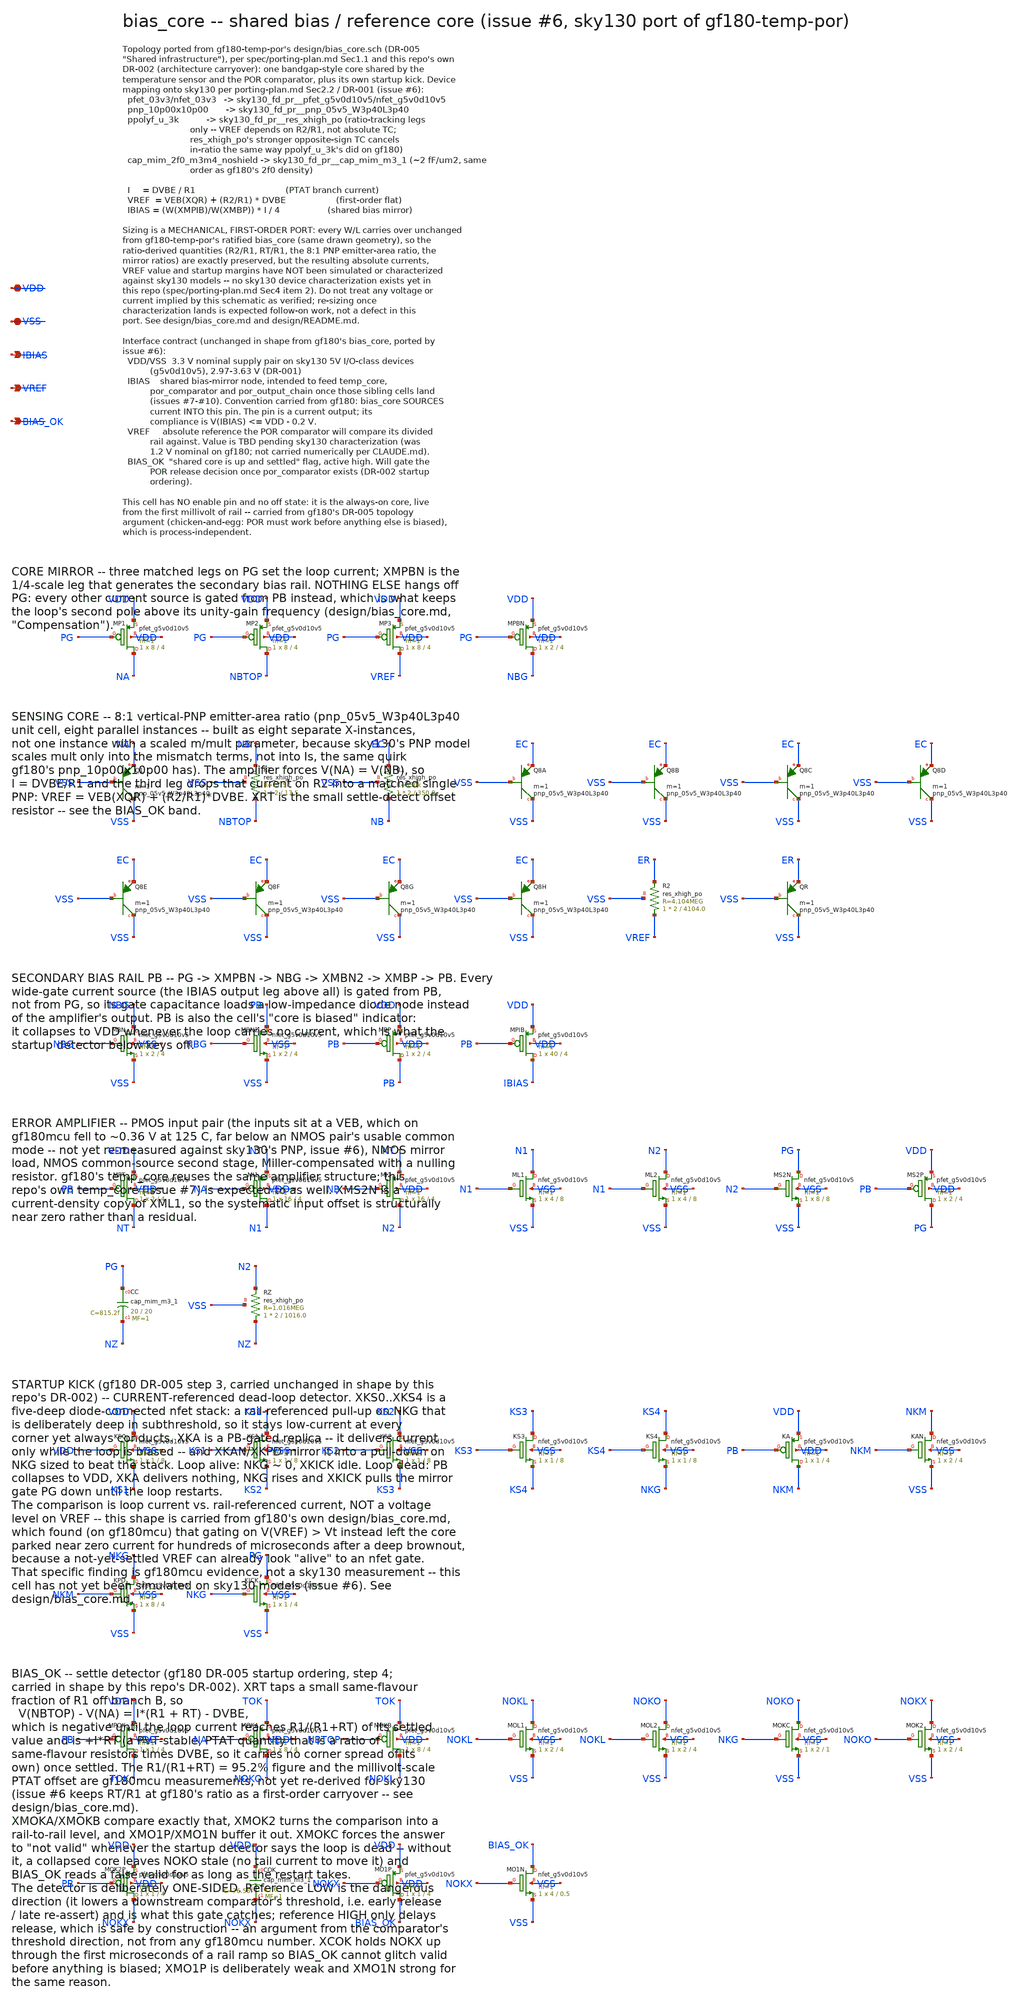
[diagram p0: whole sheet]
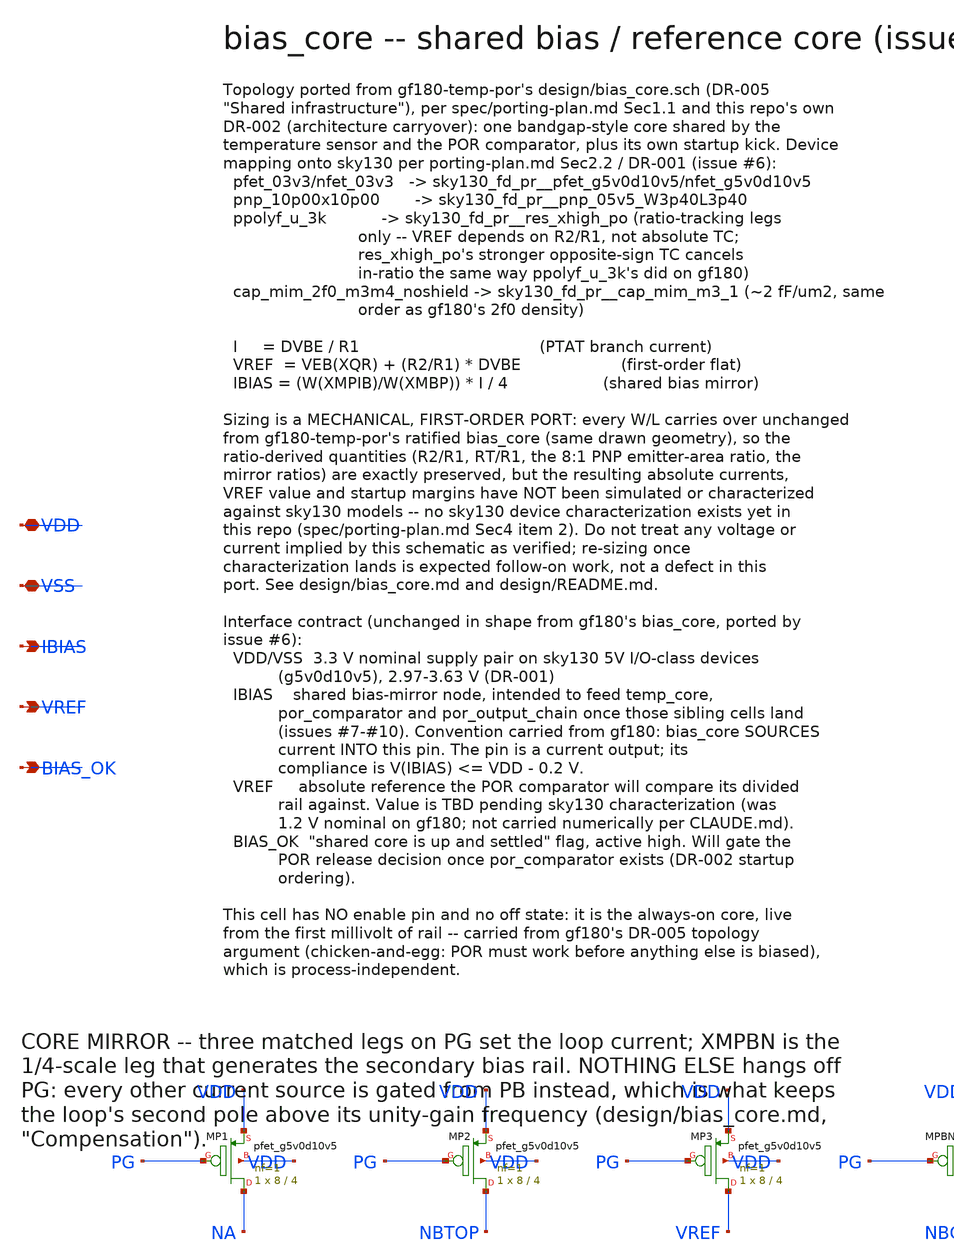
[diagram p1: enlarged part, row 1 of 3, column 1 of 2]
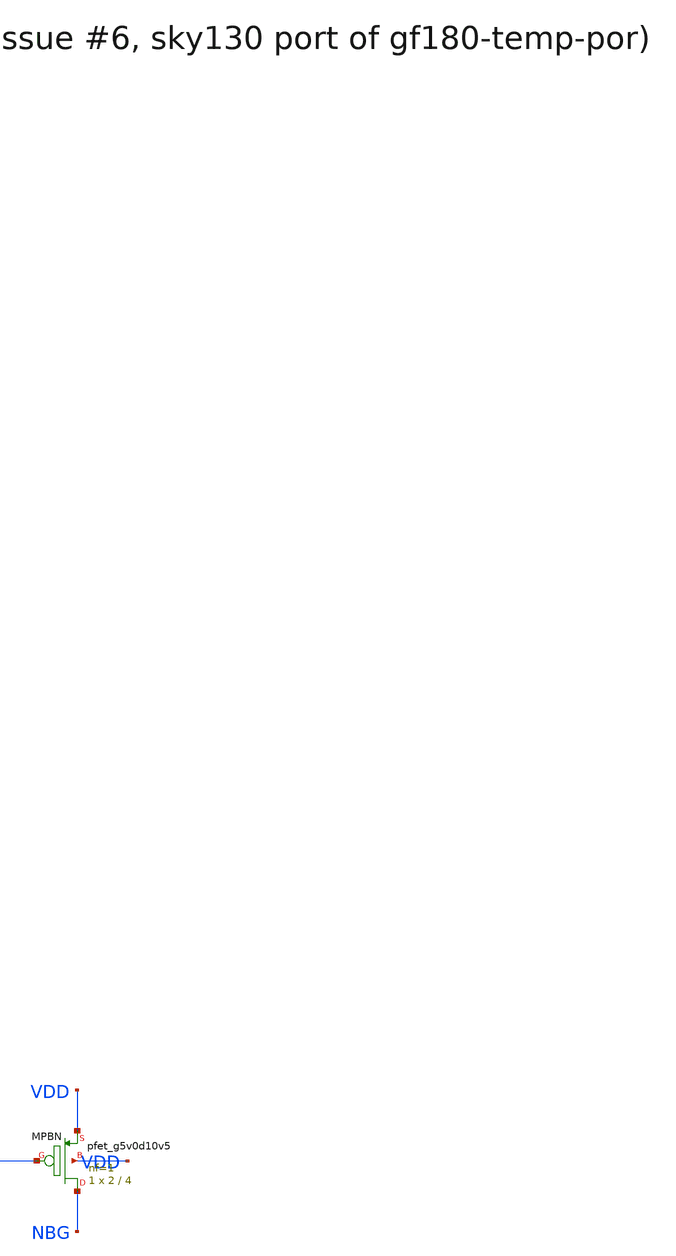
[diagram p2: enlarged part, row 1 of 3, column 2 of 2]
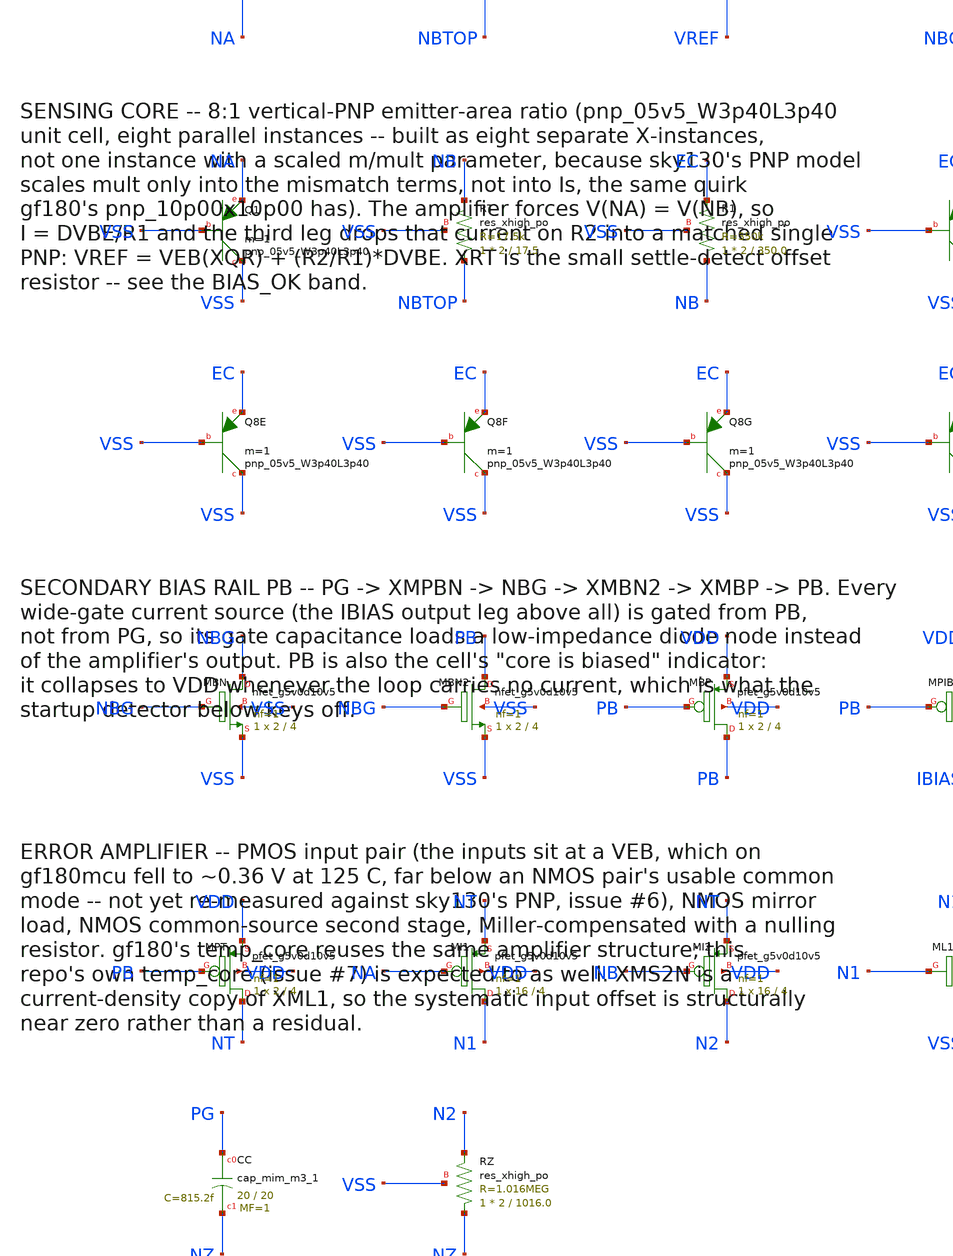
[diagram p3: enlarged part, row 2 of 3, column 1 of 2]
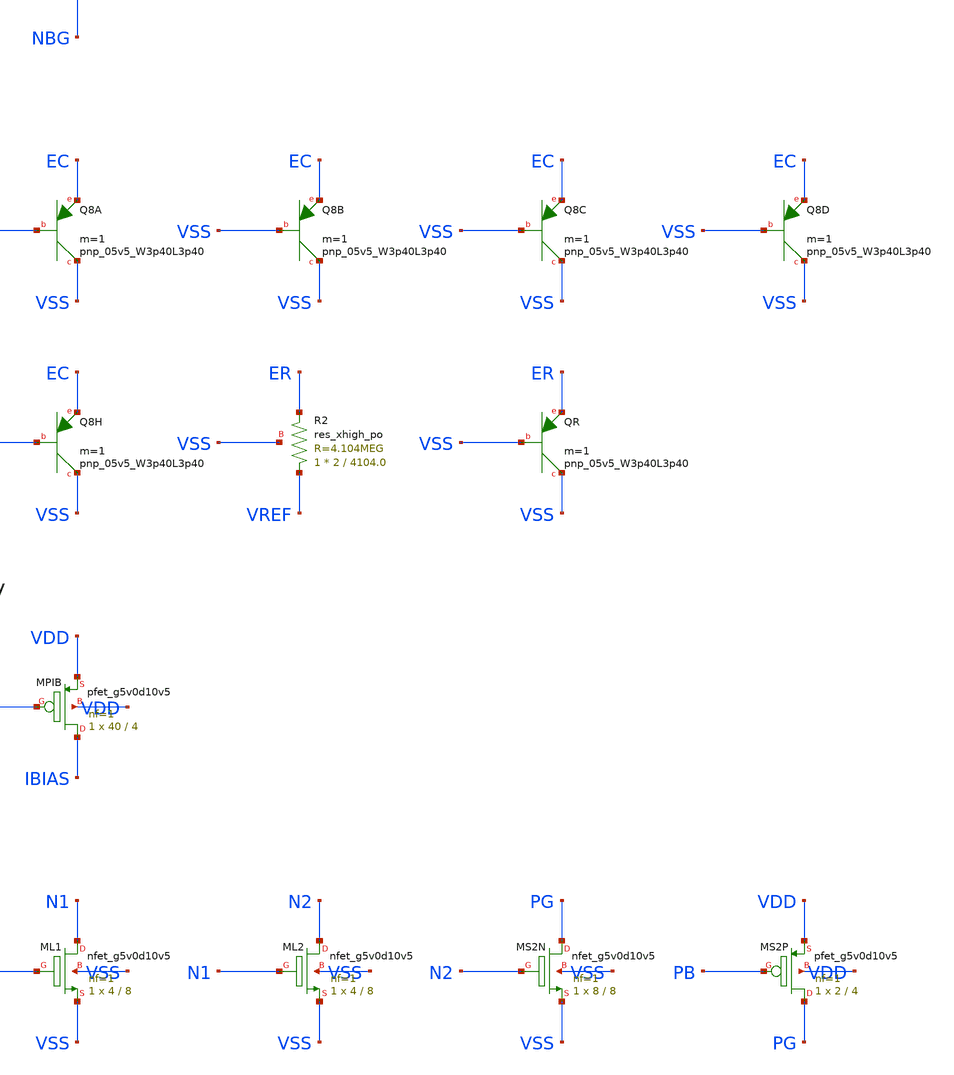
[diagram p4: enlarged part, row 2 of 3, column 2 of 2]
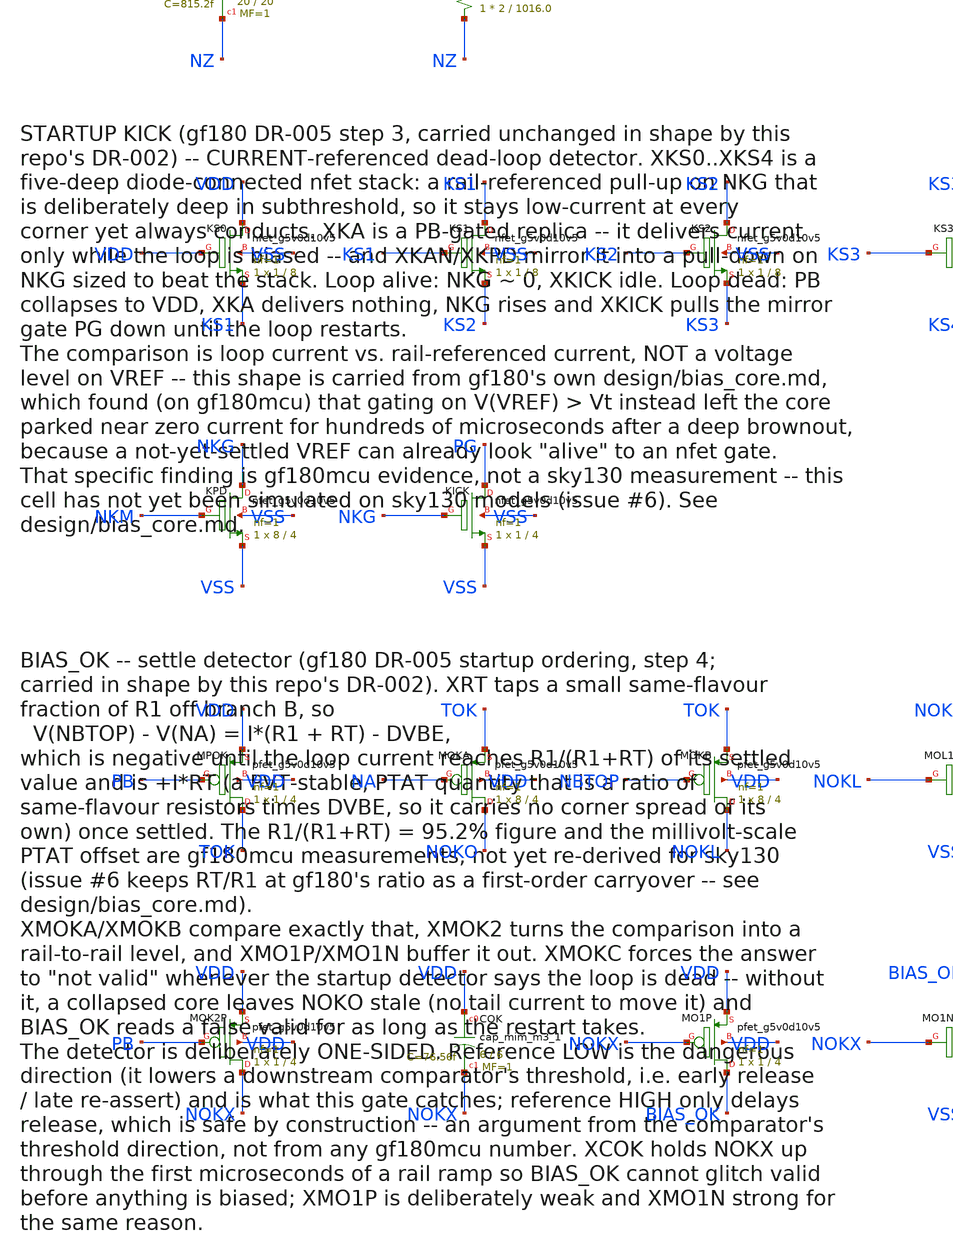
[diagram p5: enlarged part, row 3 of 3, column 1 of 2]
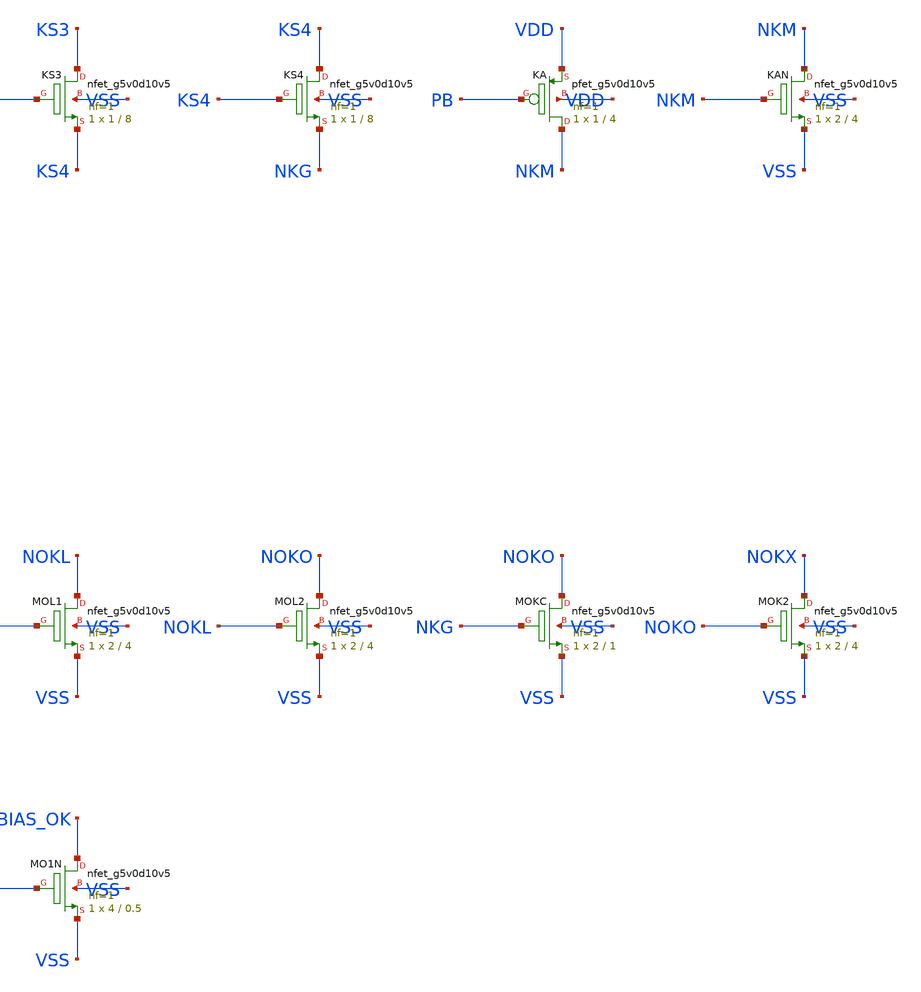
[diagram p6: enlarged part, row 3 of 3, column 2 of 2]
** sch_path: design/bias_core.sch
**.subckt bias_core VDD VSS IBIAS VREF BIAS_OK
*.iopin VDD
*.iopin VSS
*.opin IBIAS
*.opin VREF
*.opin BIAS_OK
XMP1 NA PG VDD VDD sky130_fd_pr__pfet_g5v0d10v5 L=4 W=8 nf=1 ad='int((1 + 1)/2) * 8 / 1 * 0.29' as='int((1 + 2)/2) * 8 / 1 * 0.29'
+ pd='2*int((1 + 1)/2) * (8 / 1 + 0.29)' ps='2*int((1 + 2)/2) * (8 / 1 + 0.29)' nrd='0.29 / 8 ' nrs='0.29 / 8 '
+ sa=0 sb=0 sd=0 mult=1 m=1
XMP2 NBTOP PG VDD VDD sky130_fd_pr__pfet_g5v0d10v5 L=4 W=8 nf=1 ad='int((1 + 1)/2) * 8 / 1 * 0.29' as='int((1 + 2)/2) * 8 / 1 * 0.29'
+ pd='2*int((1 + 1)/2) * (8 / 1 + 0.29)' ps='2*int((1 + 2)/2) * (8 / 1 + 0.29)' nrd='0.29 / 8 ' nrs='0.29 / 8 '
+ sa=0 sb=0 sd=0 mult=1 m=1
XMP3 VREF PG VDD VDD sky130_fd_pr__pfet_g5v0d10v5 L=4 W=8 nf=1 ad='int((1 + 1)/2) * 8 / 1 * 0.29' as='int((1 + 2)/2) * 8 / 1 * 0.29'
+ pd='2*int((1 + 1)/2) * (8 / 1 + 0.29)' ps='2*int((1 + 2)/2) * (8 / 1 + 0.29)' nrd='0.29 / 8 ' nrs='0.29 / 8 '
+ sa=0 sb=0 sd=0 mult=1 m=1
XMPBN NBG PG VDD VDD sky130_fd_pr__pfet_g5v0d10v5 L=4 W=2 nf=1 ad='int((1 + 1)/2) * 2 / 1 * 0.29' as='int((1 + 2)/2) * 2 / 1 * 0.29'
+ pd='2*int((1 + 1)/2) * (2 / 1 + 0.29)' ps='2*int((1 + 2)/2) * (2 / 1 + 0.29)' nrd='0.29 / 2 ' nrs='0.29 / 2 '
+ sa=0 sb=0 sd=0 mult=1 m=1
XQ1 VSS VSS NA sky130_fd_pr__pnp_05v5_W3p40L3p40 m=1
XRT NBTOP NB VSS sky130_fd_pr__res_xhigh_po W=2 L=17.5 mult=1 m=1
XR1 NB EC VSS sky130_fd_pr__res_xhigh_po W=2 L=350.0 mult=1 m=1
XQ8A VSS VSS EC sky130_fd_pr__pnp_05v5_W3p40L3p40 m=1
XQ8B VSS VSS EC sky130_fd_pr__pnp_05v5_W3p40L3p40 m=1
XQ8C VSS VSS EC sky130_fd_pr__pnp_05v5_W3p40L3p40 m=1
XQ8D VSS VSS EC sky130_fd_pr__pnp_05v5_W3p40L3p40 m=1
XQ8E VSS VSS EC sky130_fd_pr__pnp_05v5_W3p40L3p40 m=1
XQ8F VSS VSS EC sky130_fd_pr__pnp_05v5_W3p40L3p40 m=1
XQ8G VSS VSS EC sky130_fd_pr__pnp_05v5_W3p40L3p40 m=1
XQ8H VSS VSS EC sky130_fd_pr__pnp_05v5_W3p40L3p40 m=1
XR2 VREF ER VSS sky130_fd_pr__res_xhigh_po W=2 L=4104.0 mult=1 m=1
XQR VSS VSS ER sky130_fd_pr__pnp_05v5_W3p40L3p40 m=1
XMBN NBG NBG VSS VSS sky130_fd_pr__nfet_g5v0d10v5 L=4 W=2 nf=1 ad='int((1 + 1)/2) * 2 / 1 * 0.29' as='int((1 + 2)/2) * 2 / 1 * 0.29'
+ pd='2*int((1 + 1)/2) * (2 / 1 + 0.29)' ps='2*int((1 + 2)/2) * (2 / 1 + 0.29)' nrd='0.29 / 2 ' nrs='0.29 / 2 '
+ sa=0 sb=0 sd=0 mult=1 m=1
XMBN2 PB NBG VSS VSS sky130_fd_pr__nfet_g5v0d10v5 L=4 W=2 nf=1 ad='int((1 + 1)/2) * 2 / 1 * 0.29' as='int((1 + 2)/2) * 2 / 1 * 0.29'
+ pd='2*int((1 + 1)/2) * (2 / 1 + 0.29)' ps='2*int((1 + 2)/2) * (2 / 1 + 0.29)' nrd='0.29 / 2 ' nrs='0.29 / 2 '
+ sa=0 sb=0 sd=0 mult=1 m=1
XMBP PB PB VDD VDD sky130_fd_pr__pfet_g5v0d10v5 L=4 W=2 nf=1 ad='int((1 + 1)/2) * 2 / 1 * 0.29' as='int((1 + 2)/2) * 2 / 1 * 0.29'
+ pd='2*int((1 + 1)/2) * (2 / 1 + 0.29)' ps='2*int((1 + 2)/2) * (2 / 1 + 0.29)' nrd='0.29 / 2 ' nrs='0.29 / 2 '
+ sa=0 sb=0 sd=0 mult=1 m=1
XMPIB IBIAS PB VDD VDD sky130_fd_pr__pfet_g5v0d10v5 L=4 W=40 nf=1 ad='int((1 + 1)/2) * 40 / 1 * 0.29'
+ as='int((1 + 2)/2) * 40 / 1 * 0.29' pd='2*int((1 + 1)/2) * (40 / 1 + 0.29)' ps='2*int((1 + 2)/2) * (40 / 1 + 0.29)'
+ nrd='0.29 / 40 ' nrs='0.29 / 40 ' sa=0 sb=0 sd=0 mult=1 m=1
XMPT NT PB VDD VDD sky130_fd_pr__pfet_g5v0d10v5 L=4 W=2 nf=1 ad='int((1 + 1)/2) * 2 / 1 * 0.29' as='int((1 + 2)/2) * 2 / 1 * 0.29'
+ pd='2*int((1 + 1)/2) * (2 / 1 + 0.29)' ps='2*int((1 + 2)/2) * (2 / 1 + 0.29)' nrd='0.29 / 2 ' nrs='0.29 / 2 '
+ sa=0 sb=0 sd=0 mult=1 m=1
XMI1 N1 NA NT VDD sky130_fd_pr__pfet_g5v0d10v5 L=4 W=16 nf=1 ad='int((1 + 1)/2) * 16 / 1 * 0.29' as='int((1 + 2)/2) * 16 / 1 * 0.29'
+ pd='2*int((1 + 1)/2) * (16 / 1 + 0.29)' ps='2*int((1 + 2)/2) * (16 / 1 + 0.29)' nrd='0.29 / 16 ' nrs='0.29 / 16 '
+ sa=0 sb=0 sd=0 mult=1 m=1
XMI2 N2 NB NT VDD sky130_fd_pr__pfet_g5v0d10v5 L=4 W=16 nf=1 ad='int((1 + 1)/2) * 16 / 1 * 0.29' as='int((1 + 2)/2) * 16 / 1 * 0.29'
+ pd='2*int((1 + 1)/2) * (16 / 1 + 0.29)' ps='2*int((1 + 2)/2) * (16 / 1 + 0.29)' nrd='0.29 / 16 ' nrs='0.29 / 16 '
+ sa=0 sb=0 sd=0 mult=1 m=1
XML1 N1 N1 VSS VSS sky130_fd_pr__nfet_g5v0d10v5 L=8 W=4 nf=1 ad='int((1 + 1)/2) * 4 / 1 * 0.29' as='int((1 + 2)/2) * 4 / 1 * 0.29'
+ pd='2*int((1 + 1)/2) * (4 / 1 + 0.29)' ps='2*int((1 + 2)/2) * (4 / 1 + 0.29)' nrd='0.29 / 4 ' nrs='0.29 / 4 '
+ sa=0 sb=0 sd=0 mult=1 m=1
XML2 N2 N1 VSS VSS sky130_fd_pr__nfet_g5v0d10v5 L=8 W=4 nf=1 ad='int((1 + 1)/2) * 4 / 1 * 0.29' as='int((1 + 2)/2) * 4 / 1 * 0.29'
+ pd='2*int((1 + 1)/2) * (4 / 1 + 0.29)' ps='2*int((1 + 2)/2) * (4 / 1 + 0.29)' nrd='0.29 / 4 ' nrs='0.29 / 4 '
+ sa=0 sb=0 sd=0 mult=1 m=1
XMS2N PG N2 VSS VSS sky130_fd_pr__nfet_g5v0d10v5 L=8 W=8 nf=1 ad='int((1 + 1)/2) * 8 / 1 * 0.29' as='int((1 + 2)/2) * 8 / 1 * 0.29'
+ pd='2*int((1 + 1)/2) * (8 / 1 + 0.29)' ps='2*int((1 + 2)/2) * (8 / 1 + 0.29)' nrd='0.29 / 8 ' nrs='0.29 / 8 '
+ sa=0 sb=0 sd=0 mult=1 m=1
XMS2P PG PB VDD VDD sky130_fd_pr__pfet_g5v0d10v5 L=4 W=2 nf=1 ad='int((1 + 1)/2) * 2 / 1 * 0.29' as='int((1 + 2)/2) * 2 / 1 * 0.29'
+ pd='2*int((1 + 1)/2) * (2 / 1 + 0.29)' ps='2*int((1 + 2)/2) * (2 / 1 + 0.29)' nrd='0.29 / 2 ' nrs='0.29 / 2 '
+ sa=0 sb=0 sd=0 mult=1 m=1
XCC PG NZ sky130_fd_pr__cap_mim_m3_1 W=20 L=20 MF=1 m=1
XRZ NZ N2 VSS sky130_fd_pr__res_xhigh_po W=2 L=1016.0 mult=1 m=1
XKS0 VDD VDD KS1 VSS sky130_fd_pr__nfet_g5v0d10v5 L=8 W=1 nf=1 ad='int((1 + 1)/2) * 1 / 1 * 0.29' as='int((1 + 2)/2) * 1 / 1 * 0.29'
+ pd='2*int((1 + 1)/2) * (1 / 1 + 0.29)' ps='2*int((1 + 2)/2) * (1 / 1 + 0.29)' nrd='0.29 / 1 ' nrs='0.29 / 1 '
+ sa=0 sb=0 sd=0 mult=1 m=1
XKS1 KS1 KS1 KS2 VSS sky130_fd_pr__nfet_g5v0d10v5 L=8 W=1 nf=1 ad='int((1 + 1)/2) * 1 / 1 * 0.29' as='int((1 + 2)/2) * 1 / 1 * 0.29'
+ pd='2*int((1 + 1)/2) * (1 / 1 + 0.29)' ps='2*int((1 + 2)/2) * (1 / 1 + 0.29)' nrd='0.29 / 1 ' nrs='0.29 / 1 '
+ sa=0 sb=0 sd=0 mult=1 m=1
XKS2 KS2 KS2 KS3 VSS sky130_fd_pr__nfet_g5v0d10v5 L=8 W=1 nf=1 ad='int((1 + 1)/2) * 1 / 1 * 0.29' as='int((1 + 2)/2) * 1 / 1 * 0.29'
+ pd='2*int((1 + 1)/2) * (1 / 1 + 0.29)' ps='2*int((1 + 2)/2) * (1 / 1 + 0.29)' nrd='0.29 / 1 ' nrs='0.29 / 1 '
+ sa=0 sb=0 sd=0 mult=1 m=1
XKS3 KS3 KS3 KS4 VSS sky130_fd_pr__nfet_g5v0d10v5 L=8 W=1 nf=1 ad='int((1 + 1)/2) * 1 / 1 * 0.29' as='int((1 + 2)/2) * 1 / 1 * 0.29'
+ pd='2*int((1 + 1)/2) * (1 / 1 + 0.29)' ps='2*int((1 + 2)/2) * (1 / 1 + 0.29)' nrd='0.29 / 1 ' nrs='0.29 / 1 '
+ sa=0 sb=0 sd=0 mult=1 m=1
XKS4 KS4 KS4 NKG VSS sky130_fd_pr__nfet_g5v0d10v5 L=8 W=1 nf=1 ad='int((1 + 1)/2) * 1 / 1 * 0.29' as='int((1 + 2)/2) * 1 / 1 * 0.29'
+ pd='2*int((1 + 1)/2) * (1 / 1 + 0.29)' ps='2*int((1 + 2)/2) * (1 / 1 + 0.29)' nrd='0.29 / 1 ' nrs='0.29 / 1 '
+ sa=0 sb=0 sd=0 mult=1 m=1
XKA NKM PB VDD VDD sky130_fd_pr__pfet_g5v0d10v5 L=4 W=1 nf=1 ad='int((1 + 1)/2) * 1 / 1 * 0.29' as='int((1 + 2)/2) * 1 / 1 * 0.29'
+ pd='2*int((1 + 1)/2) * (1 / 1 + 0.29)' ps='2*int((1 + 2)/2) * (1 / 1 + 0.29)' nrd='0.29 / 1 ' nrs='0.29 / 1 '
+ sa=0 sb=0 sd=0 mult=1 m=1
XKAN NKM NKM VSS VSS sky130_fd_pr__nfet_g5v0d10v5 L=4 W=2 nf=1 ad='int((1 + 1)/2) * 2 / 1 * 0.29' as='int((1 + 2)/2) * 2 / 1 * 0.29'
+ pd='2*int((1 + 1)/2) * (2 / 1 + 0.29)' ps='2*int((1 + 2)/2) * (2 / 1 + 0.29)' nrd='0.29 / 2 ' nrs='0.29 / 2 '
+ sa=0 sb=0 sd=0 mult=1 m=1
XKPD NKG NKM VSS VSS sky130_fd_pr__nfet_g5v0d10v5 L=4 W=8 nf=1 ad='int((1 + 1)/2) * 8 / 1 * 0.29' as='int((1 + 2)/2) * 8 / 1 * 0.29'
+ pd='2*int((1 + 1)/2) * (8 / 1 + 0.29)' ps='2*int((1 + 2)/2) * (8 / 1 + 0.29)' nrd='0.29 / 8 ' nrs='0.29 / 8 '
+ sa=0 sb=0 sd=0 mult=1 m=1
XKICK PG NKG VSS VSS sky130_fd_pr__nfet_g5v0d10v5 L=4 W=1 nf=1 ad='int((1 + 1)/2) * 1 / 1 * 0.29' as='int((1 + 2)/2) * 1 / 1 * 0.29'
+ pd='2*int((1 + 1)/2) * (1 / 1 + 0.29)' ps='2*int((1 + 2)/2) * (1 / 1 + 0.29)' nrd='0.29 / 1 ' nrs='0.29 / 1 '
+ sa=0 sb=0 sd=0 mult=1 m=1
XMPOK TOK PB VDD VDD sky130_fd_pr__pfet_g5v0d10v5 L=4 W=1 nf=1 ad='int((1 + 1)/2) * 1 / 1 * 0.29' as='int((1 + 2)/2) * 1 / 1 * 0.29'
+ pd='2*int((1 + 1)/2) * (1 / 1 + 0.29)' ps='2*int((1 + 2)/2) * (1 / 1 + 0.29)' nrd='0.29 / 1 ' nrs='0.29 / 1 '
+ sa=0 sb=0 sd=0 mult=1 m=1
XMOKA NOKO NA TOK VDD sky130_fd_pr__pfet_g5v0d10v5 L=4 W=8 nf=1 ad='int((1 + 1)/2) * 8 / 1 * 0.29' as='int((1 + 2)/2) * 8 / 1 * 0.29'
+ pd='2*int((1 + 1)/2) * (8 / 1 + 0.29)' ps='2*int((1 + 2)/2) * (8 / 1 + 0.29)' nrd='0.29 / 8 ' nrs='0.29 / 8 '
+ sa=0 sb=0 sd=0 mult=1 m=1
XMOKB NOKL NBTOP TOK VDD sky130_fd_pr__pfet_g5v0d10v5 L=4 W=8 nf=1 ad='int((1 + 1)/2) * 8 / 1 * 0.29'
+ as='int((1 + 2)/2) * 8 / 1 * 0.29' pd='2*int((1 + 1)/2) * (8 / 1 + 0.29)' ps='2*int((1 + 2)/2) * (8 / 1 + 0.29)'
+ nrd='0.29 / 8 ' nrs='0.29 / 8 ' sa=0 sb=0 sd=0 mult=1 m=1
XMOL1 NOKL NOKL VSS VSS sky130_fd_pr__nfet_g5v0d10v5 L=4 W=2 nf=1 ad='int((1 + 1)/2) * 2 / 1 * 0.29'
+ as='int((1 + 2)/2) * 2 / 1 * 0.29' pd='2*int((1 + 1)/2) * (2 / 1 + 0.29)' ps='2*int((1 + 2)/2) * (2 / 1 + 0.29)'
+ nrd='0.29 / 2 ' nrs='0.29 / 2 ' sa=0 sb=0 sd=0 mult=1 m=1
XMOL2 NOKO NOKL VSS VSS sky130_fd_pr__nfet_g5v0d10v5 L=4 W=2 nf=1 ad='int((1 + 1)/2) * 2 / 1 * 0.29'
+ as='int((1 + 2)/2) * 2 / 1 * 0.29' pd='2*int((1 + 1)/2) * (2 / 1 + 0.29)' ps='2*int((1 + 2)/2) * (2 / 1 + 0.29)'
+ nrd='0.29 / 2 ' nrs='0.29 / 2 ' sa=0 sb=0 sd=0 mult=1 m=1
XMOKC NOKO NKG VSS VSS sky130_fd_pr__nfet_g5v0d10v5 L=1 W=2 nf=1 ad='int((1 + 1)/2) * 2 / 1 * 0.29' as='int((1 + 2)/2) * 2 / 1 * 0.29'
+ pd='2*int((1 + 1)/2) * (2 / 1 + 0.29)' ps='2*int((1 + 2)/2) * (2 / 1 + 0.29)' nrd='0.29 / 2 ' nrs='0.29 / 2 '
+ sa=0 sb=0 sd=0 mult=1 m=1
XMOK2 NOKX NOKO VSS VSS sky130_fd_pr__nfet_g5v0d10v5 L=4 W=2 nf=1 ad='int((1 + 1)/2) * 2 / 1 * 0.29'
+ as='int((1 + 2)/2) * 2 / 1 * 0.29' pd='2*int((1 + 1)/2) * (2 / 1 + 0.29)' ps='2*int((1 + 2)/2) * (2 / 1 + 0.29)'
+ nrd='0.29 / 2 ' nrs='0.29 / 2 ' sa=0 sb=0 sd=0 mult=1 m=1
XMOK2P NOKX PB VDD VDD sky130_fd_pr__pfet_g5v0d10v5 L=4 W=1 nf=1 ad='int((1 + 1)/2) * 1 / 1 * 0.29' as='int((1 + 2)/2) * 1 / 1 * 0.29'
+ pd='2*int((1 + 1)/2) * (1 / 1 + 0.29)' ps='2*int((1 + 2)/2) * (1 / 1 + 0.29)' nrd='0.29 / 1 ' nrs='0.29 / 1 '
+ sa=0 sb=0 sd=0 mult=1 m=1
XCOK VDD NOKX sky130_fd_pr__cap_mim_m3_1 W=6 L=6 MF=1 m=1
XMO1P BIAS_OK NOKX VDD VDD sky130_fd_pr__pfet_g5v0d10v5 L=4 W=1 nf=1 ad='int((1 + 1)/2) * 1 / 1 * 0.29'
+ as='int((1 + 2)/2) * 1 / 1 * 0.29' pd='2*int((1 + 1)/2) * (1 / 1 + 0.29)' ps='2*int((1 + 2)/2) * (1 / 1 + 0.29)'
+ nrd='0.29 / 1 ' nrs='0.29 / 1 ' sa=0 sb=0 sd=0 mult=1 m=1
XMO1N BIAS_OK NOKX VSS VSS sky130_fd_pr__nfet_g5v0d10v5 L=0.5 W=4 nf=1 ad='int((1 + 1)/2) * 4 / 1 * 0.29'
+ as='int((1 + 2)/2) * 4 / 1 * 0.29' pd='2*int((1 + 1)/2) * (4 / 1 + 0.29)' ps='2*int((1 + 2)/2) * (4 / 1 + 0.29)'
+ nrd='0.29 / 4 ' nrs='0.29 / 4 ' sa=0 sb=0 sd=0 mult=1 m=1
**.ends
.end
